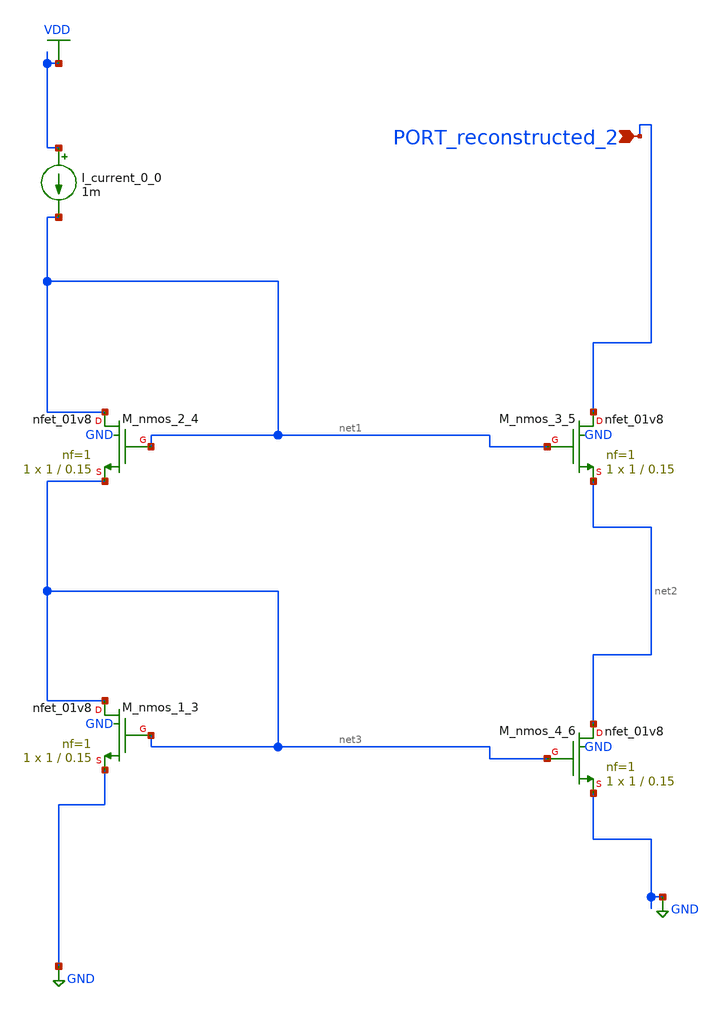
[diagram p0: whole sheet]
** sch_path: schematics/AMSNet/259.sch
**.subckt 259 PORT_reconstructed_2
*.ipin PORT_reconstructed_2
I_current_0_0 VDD net1 1m
XM_nmos_1_3 net3 net3 GND GND sky130_fd_pr__nfet_01v8 L=0.15 W=1 nf=1 ad='int((1 + 1)/2) * 1 / 1 * 0.29'
+ as='int((1 + 2)/2) * 1 / 1 * 0.29' pd='2*int((1 + 1)/2) * (1 / 1 + 0.29)' ps='2*int((1 + 2)/2) * (1 / 1 + 0.29)'
+ nrd='0.29 / 1 ' nrs='0.29 / 1 ' sa=0 sb=0 sd=0 mult=1 m=1
XM_nmos_2_4 net1 net1 net3 GND sky130_fd_pr__nfet_01v8 L=0.15 W=1 nf=1 ad='int((1 + 1)/2) * 1 / 1 * 0.29'
+ as='int((1 + 2)/2) * 1 / 1 * 0.29' pd='2*int((1 + 1)/2) * (1 / 1 + 0.29)' ps='2*int((1 + 2)/2) * (1 / 1 + 0.29)'
+ nrd='0.29 / 1 ' nrs='0.29 / 1 ' sa=0 sb=0 sd=0 mult=1 m=1
XM_nmos_3_5 PORT_reconstructed_2 net1 net2 GND sky130_fd_pr__nfet_01v8 L=0.15 W=1 nf=1 ad='int((1 + 1)/2) * 1 / 1 * 0.29'
+ as='int((1 + 2)/2) * 1 / 1 * 0.29' pd='2*int((1 + 1)/2) * (1 / 1 + 0.29)' ps='2*int((1 + 2)/2) * (1 / 1 + 0.29)'
+ nrd='0.29 / 1 ' nrs='0.29 / 1 ' sa=0 sb=0 sd=0 mult=1 m=1
XM_nmos_4_6 net2 net3 GND GND sky130_fd_pr__nfet_01v8 L=0.15 W=1 nf=1 ad='int((1 + 1)/2) * 1 / 1 * 0.29'
+ as='int((1 + 2)/2) * 1 / 1 * 0.29' pd='2*int((1 + 1)/2) * (1 / 1 + 0.29)' ps='2*int((1 + 2)/2) * (1 / 1 + 0.29)'
+ nrd='0.29 / 1 ' nrs='0.29 / 1 ' sa=0 sb=0 sd=0 mult=1 m=1
**.ends
.GLOBAL GND
.GLOBAL VDD
.end
